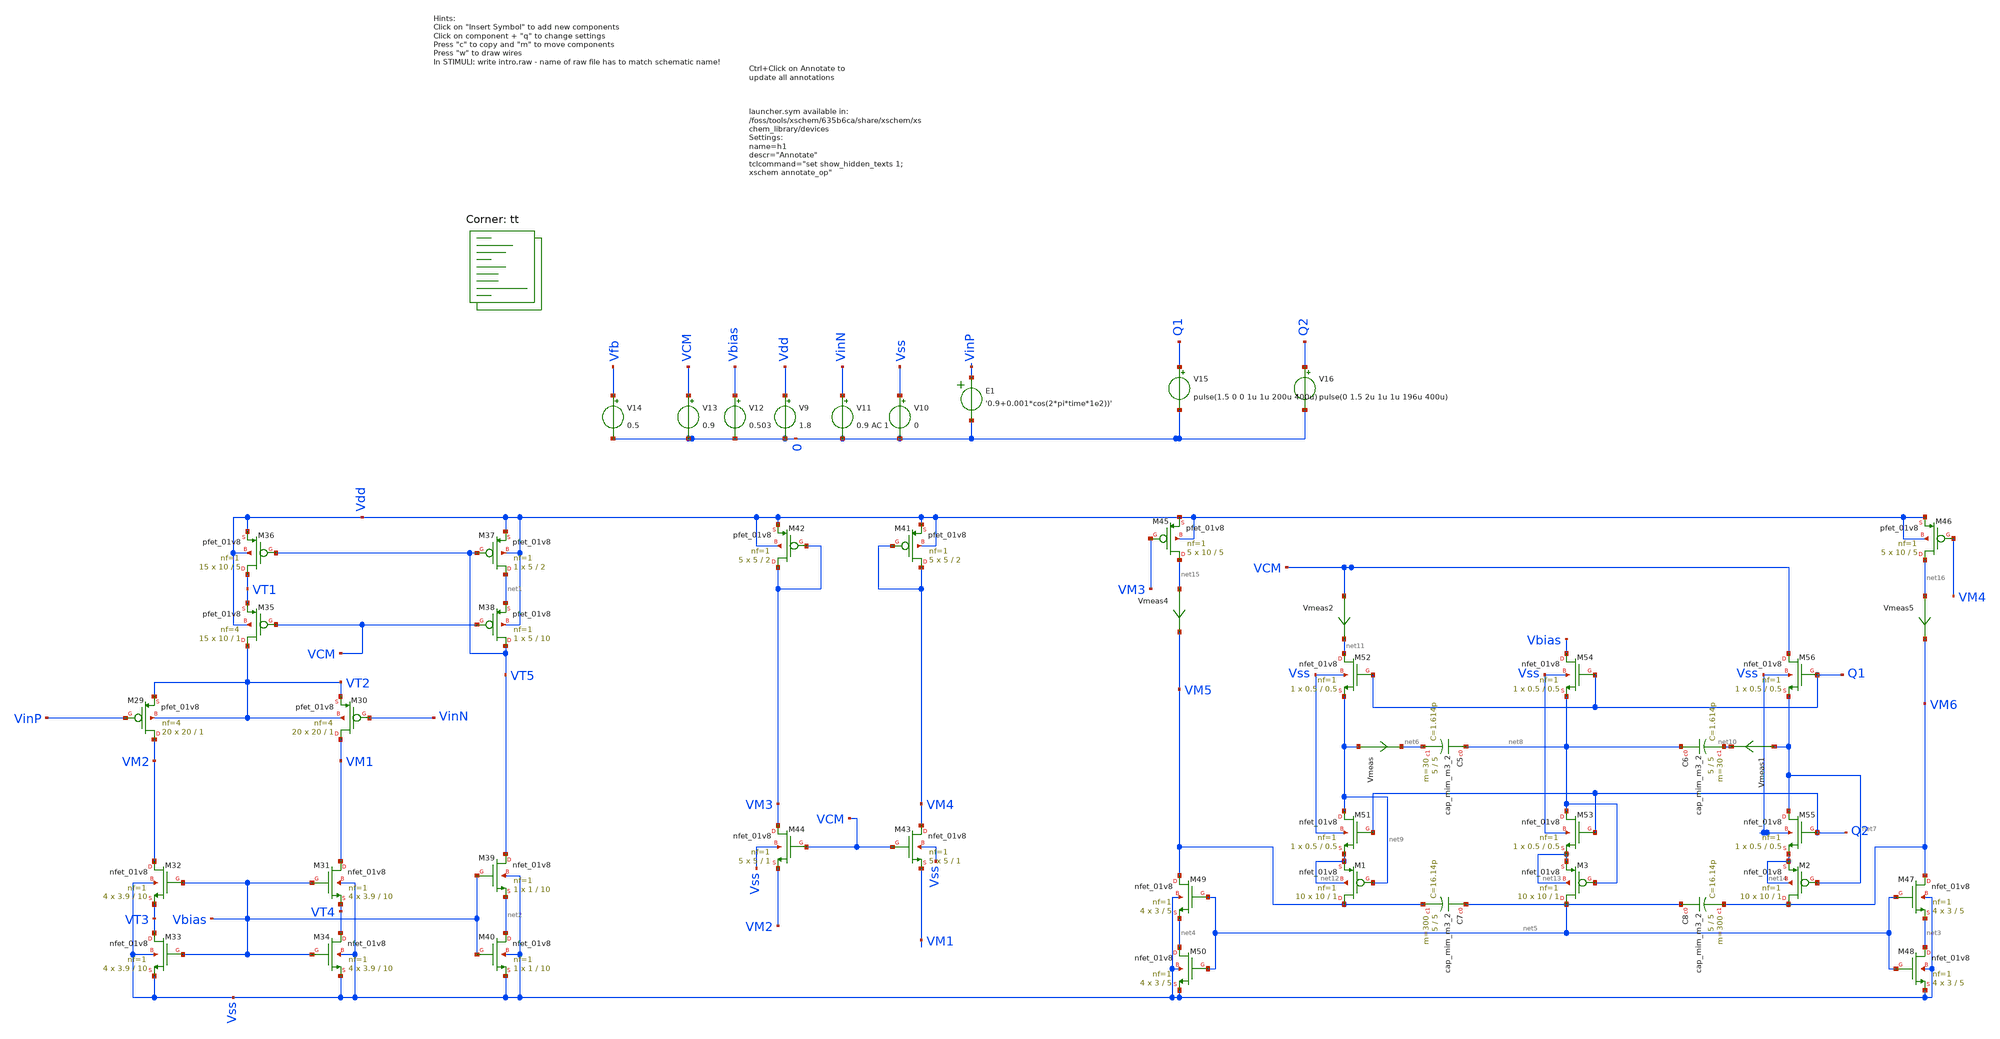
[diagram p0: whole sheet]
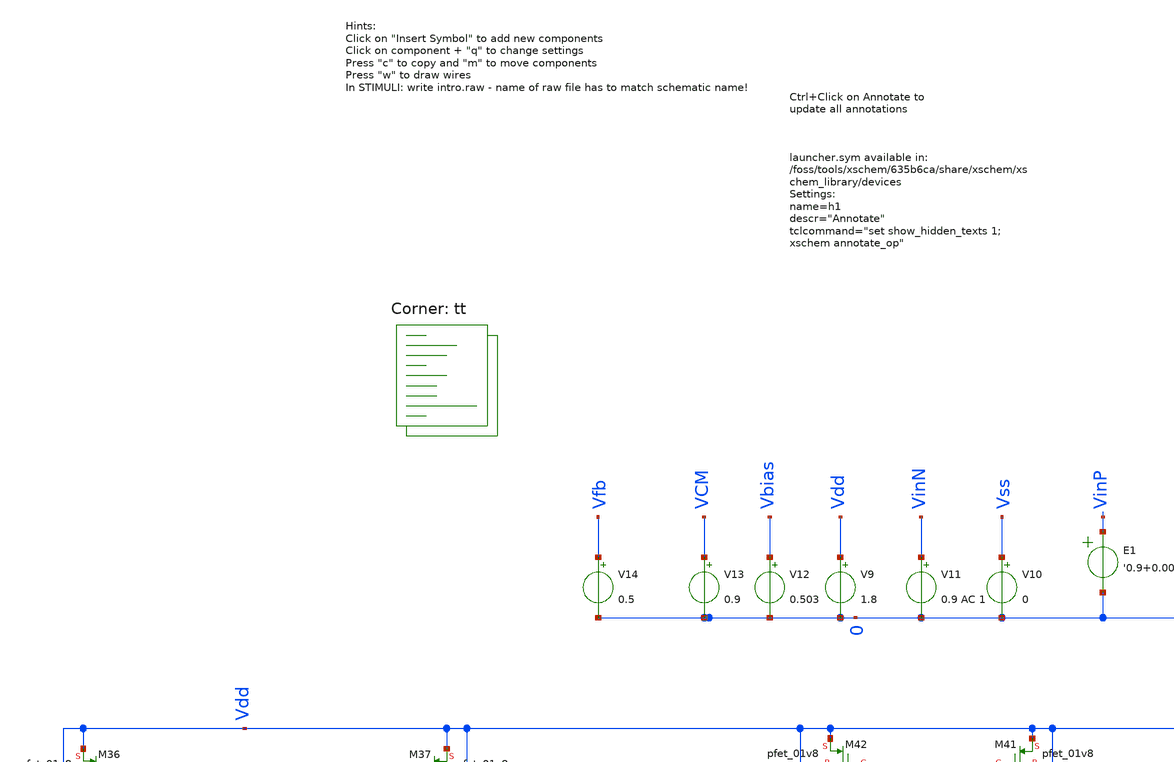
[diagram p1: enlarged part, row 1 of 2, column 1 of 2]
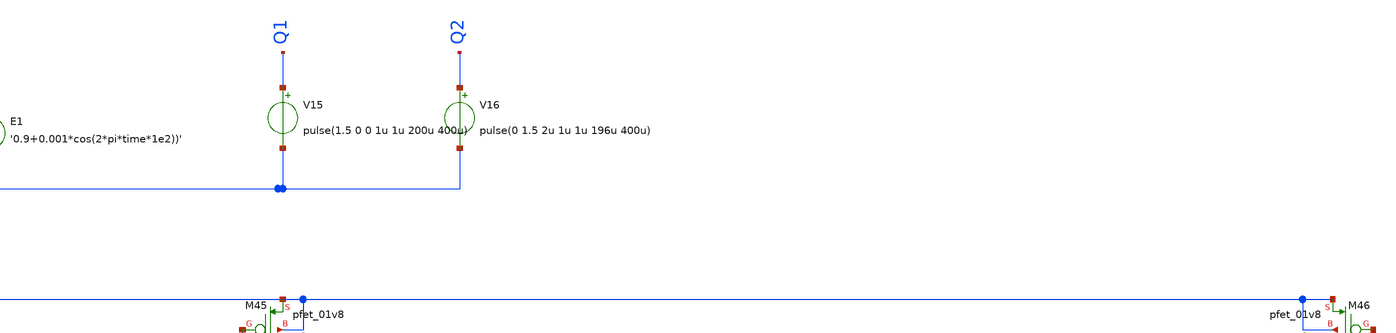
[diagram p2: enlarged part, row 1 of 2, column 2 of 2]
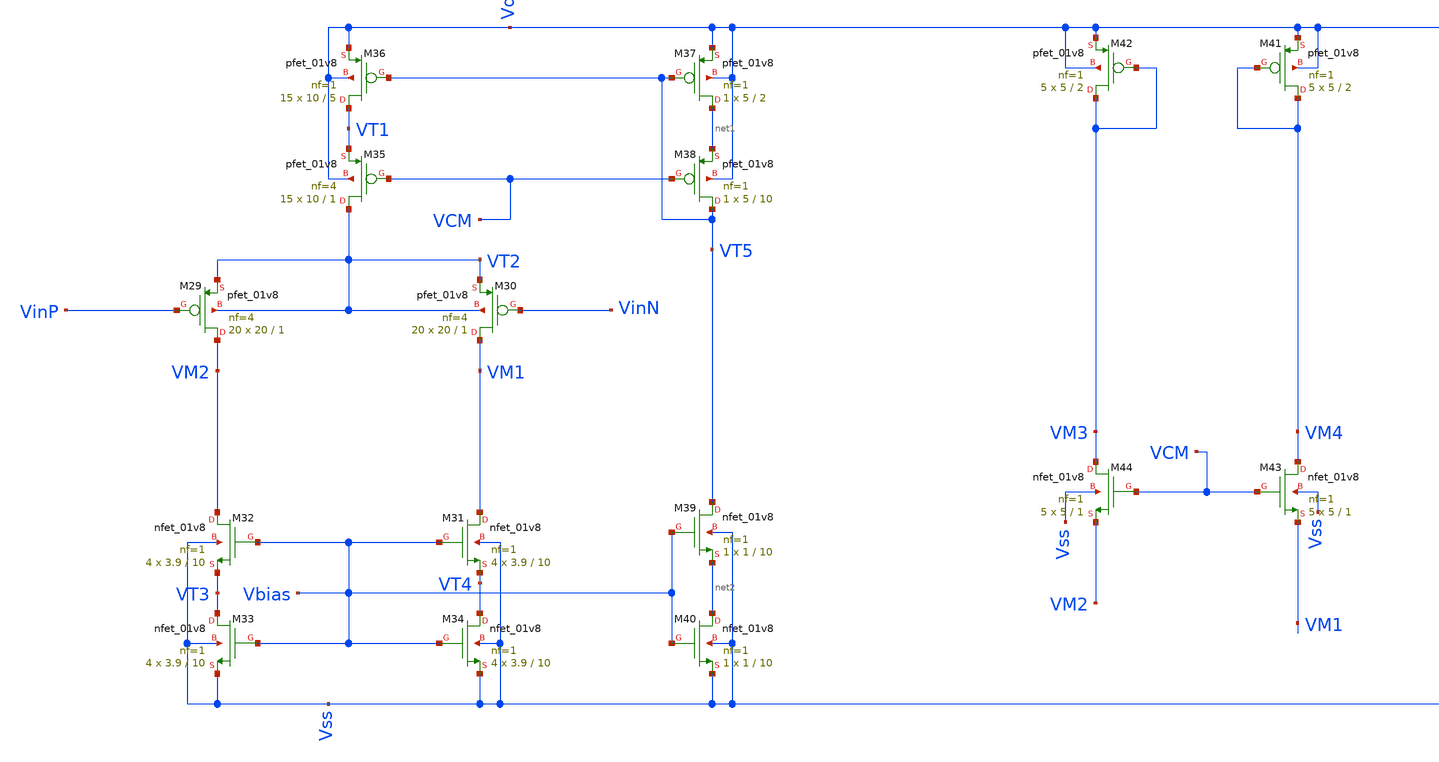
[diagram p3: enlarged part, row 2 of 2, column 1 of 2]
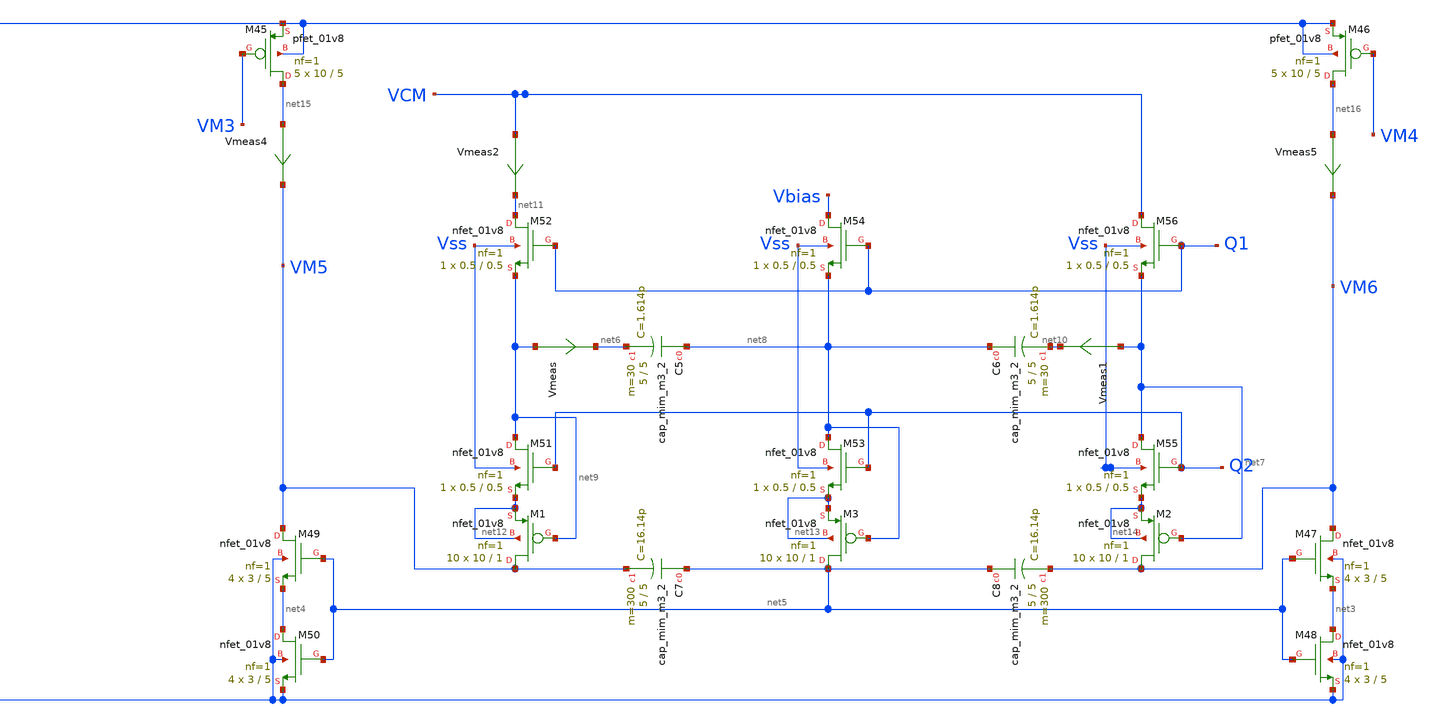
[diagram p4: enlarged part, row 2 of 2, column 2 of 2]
** sch_path: backup2.sch
**.subckt backup2
XM29 VM2 VinP VT2 VT2 sky130_fd_pr__pfet_01v8 L=1 W=20 nf=4 ad='int((nf+1)/2) * W/nf * 0.29' as='int((nf+2)/2) * W/nf * 0.29'
+ pd='2*int((nf+1)/2) * (W/nf + 0.29)' ps='2*int((nf+2)/2) * (W/nf + 0.29)' nrd='0.29 / W' nrs='0.29 / W'
+ sa=0 sb=0 sd=0 mult=20 m=20
XM30 VM1 VinN VT2 VT2 sky130_fd_pr__pfet_01v8 L=1 W=20 nf=4 ad='int((nf+1)/2) * W/nf * 0.29' as='int((nf+2)/2) * W/nf * 0.29'
+ pd='2*int((nf+1)/2) * (W/nf + 0.29)' ps='2*int((nf+2)/2) * (W/nf + 0.29)' nrd='0.29 / W' nrs='0.29 / W'
+ sa=0 sb=0 sd=0 mult=20 m=20
XM31 VM1 Vbias VT4 Vss sky130_fd_pr__nfet_01v8 L=10 W=3.9 nf=1 ad='int((nf+1)/2) * W/nf * 0.29' as='int((nf+2)/2) * W/nf * 0.29'
+ pd='2*int((nf+1)/2) * (W/nf + 0.29)' ps='2*int((nf+2)/2) * (W/nf + 0.29)' nrd='0.29 / W' nrs='0.29 / W'
+ sa=0 sb=0 sd=0 mult=4 m=4
XM32 VM2 Vbias VT3 Vss sky130_fd_pr__nfet_01v8 L=10 W=3.9 nf=1 ad='int((nf+1)/2) * W/nf * 0.29' as='int((nf+2)/2) * W/nf * 0.29'
+ pd='2*int((nf+1)/2) * (W/nf + 0.29)' ps='2*int((nf+2)/2) * (W/nf + 0.29)' nrd='0.29 / W' nrs='0.29 / W'
+ sa=0 sb=0 sd=0 mult=4 m=4
XM33 VT3 Vbias Vss Vss sky130_fd_pr__nfet_01v8 L=10 W=3.9 nf=1 ad='int((nf+1)/2) * W/nf * 0.29' as='int((nf+2)/2) * W/nf * 0.29'
+ pd='2*int((nf+1)/2) * (W/nf + 0.29)' ps='2*int((nf+2)/2) * (W/nf + 0.29)' nrd='0.29 / W' nrs='0.29 / W'
+ sa=0 sb=0 sd=0 mult=4 m=4
XM34 VT4 Vbias Vss Vss sky130_fd_pr__nfet_01v8 L=10 W=3.9 nf=1 ad='int((nf+1)/2) * W/nf * 0.29' as='int((nf+2)/2) * W/nf * 0.29'
+ pd='2*int((nf+1)/2) * (W/nf + 0.29)' ps='2*int((nf+2)/2) * (W/nf + 0.29)' nrd='0.29 / W' nrs='0.29 / W'
+ sa=0 sb=0 sd=0 mult=4 m=4
XM35 VT2 VCM VT1 Vdd sky130_fd_pr__pfet_01v8 L=1 W=10 nf=4 ad='int((nf+1)/2) * W/nf * 0.29' as='int((nf+2)/2) * W/nf * 0.29'
+ pd='2*int((nf+1)/2) * (W/nf + 0.29)' ps='2*int((nf+2)/2) * (W/nf + 0.29)' nrd='0.29 / W' nrs='0.29 / W'
+ sa=0 sb=0 sd=0 mult=15 m=15
XM36 VT1 VT5 Vdd Vdd sky130_fd_pr__pfet_01v8 L=5 W=10 nf=1 ad='int((nf+1)/2) * W/nf * 0.29' as='int((nf+2)/2) * W/nf * 0.29'
+ pd='2*int((nf+1)/2) * (W/nf + 0.29)' ps='2*int((nf+2)/2) * (W/nf + 0.29)' nrd='0.29 / W' nrs='0.29 / W'
+ sa=0 sb=0 sd=0 mult=15 m=15
XM37 net1 VT5 Vdd Vdd sky130_fd_pr__pfet_01v8 L=2 W=5 nf=1 ad='int((nf+1)/2) * W/nf * 0.29' as='int((nf+2)/2) * W/nf * 0.29'
+ pd='2*int((nf+1)/2) * (W/nf + 0.29)' ps='2*int((nf+2)/2) * (W/nf + 0.29)' nrd='0.29 / W' nrs='0.29 / W'
+ sa=0 sb=0 sd=0 mult=1 m=1
XM38 VT5 VCM net1 Vdd sky130_fd_pr__pfet_01v8 L=10 W=5 nf=1 ad='int((nf+1)/2) * W/nf * 0.29' as='int((nf+2)/2) * W/nf * 0.29'
+ pd='2*int((nf+1)/2) * (W/nf + 0.29)' ps='2*int((nf+2)/2) * (W/nf + 0.29)' nrd='0.29 / W' nrs='0.29 / W'
+ sa=0 sb=0 sd=0 mult=1 m=1
XM39 VT5 Vbias net2 Vss sky130_fd_pr__nfet_01v8 L=10 W=1 nf=1 ad='int((nf+1)/2) * W/nf * 0.29' as='int((nf+2)/2) * W/nf * 0.29'
+ pd='2*int((nf+1)/2) * (W/nf + 0.29)' ps='2*int((nf+2)/2) * (W/nf + 0.29)' nrd='0.29 / W' nrs='0.29 / W'
+ sa=0 sb=0 sd=0 mult=1 m=1
XM40 net2 Vbias Vss Vss sky130_fd_pr__nfet_01v8 L=10 W=1 nf=1 ad='int((nf+1)/2) * W/nf * 0.29' as='int((nf+2)/2) * W/nf * 0.29'
+ pd='2*int((nf+1)/2) * (W/nf + 0.29)' ps='2*int((nf+2)/2) * (W/nf + 0.29)' nrd='0.29 / W' nrs='0.29 / W'
+ sa=0 sb=0 sd=0 mult=1 m=1
XM41 VM4 VM4 Vdd Vdd sky130_fd_pr__pfet_01v8 L=2 W=5 nf=1 ad='int((nf+1)/2) * W/nf * 0.29' as='int((nf+2)/2) * W/nf * 0.29'
+ pd='2*int((nf+1)/2) * (W/nf + 0.29)' ps='2*int((nf+2)/2) * (W/nf + 0.29)' nrd='0.29 / W' nrs='0.29 / W'
+ sa=0 sb=0 sd=0 mult=5 m=5
XM42 VM3 VM3 Vdd Vdd sky130_fd_pr__pfet_01v8 L=2 W=5 nf=1 ad='int((nf+1)/2) * W/nf * 0.29' as='int((nf+2)/2) * W/nf * 0.29'
+ pd='2*int((nf+1)/2) * (W/nf + 0.29)' ps='2*int((nf+2)/2) * (W/nf + 0.29)' nrd='0.29 / W' nrs='0.29 / W'
+ sa=0 sb=0 sd=0 mult=5 m=5
XM43 VM4 VCM VM1 Vss sky130_fd_pr__nfet_01v8 L=1 W=5 nf=1 ad='int((nf+1)/2) * W/nf * 0.29' as='int((nf+2)/2) * W/nf * 0.29'
+ pd='2*int((nf+1)/2) * (W/nf + 0.29)' ps='2*int((nf+2)/2) * (W/nf + 0.29)' nrd='0.29 / W' nrs='0.29 / W'
+ sa=0 sb=0 sd=0 mult=5 m=5
XM44 VM3 VCM VM2 Vss sky130_fd_pr__nfet_01v8 L=1 W=5 nf=1 ad='int((nf+1)/2) * W/nf * 0.29' as='int((nf+2)/2) * W/nf * 0.29'
+ pd='2*int((nf+1)/2) * (W/nf + 0.29)' ps='2*int((nf+2)/2) * (W/nf + 0.29)' nrd='0.29 / W' nrs='0.29 / W'
+ sa=0 sb=0 sd=0 mult=5 m=5
XM45 net15 VM3 Vdd Vdd sky130_fd_pr__pfet_01v8 L=5 W=10 nf=1 ad='int((nf+1)/2) * W/nf * 0.29' as='int((nf+2)/2) * W/nf * 0.29'
+ pd='2*int((nf+1)/2) * (W/nf + 0.29)' ps='2*int((nf+2)/2) * (W/nf + 0.29)' nrd='0.29 / W' nrs='0.29 / W'
+ sa=0 sb=0 sd=0 mult=5 m=5
XM46 net16 VM4 Vdd Vdd sky130_fd_pr__pfet_01v8 L=5 W=10 nf=1 ad='int((nf+1)/2) * W/nf * 0.29' as='int((nf+2)/2) * W/nf * 0.29'
+ pd='2*int((nf+1)/2) * (W/nf + 0.29)' ps='2*int((nf+2)/2) * (W/nf + 0.29)' nrd='0.29 / W' nrs='0.29 / W'
+ sa=0 sb=0 sd=0 mult=5 m=5
XM47 VM6 net5 net3 Vss sky130_fd_pr__nfet_01v8 L=5 W=3 nf=1 ad='int((nf+1)/2) * W/nf * 0.29' as='int((nf+2)/2) * W/nf * 0.29'
+ pd='2*int((nf+1)/2) * (W/nf + 0.29)' ps='2*int((nf+2)/2) * (W/nf + 0.29)' nrd='0.29 / W' nrs='0.29 / W'
+ sa=0 sb=0 sd=0 mult=4 m=4
XM48 net3 net5 Vss Vss sky130_fd_pr__nfet_01v8 L=5 W=3 nf=1 ad='int((nf+1)/2) * W/nf * 0.29' as='int((nf+2)/2) * W/nf * 0.29'
+ pd='2*int((nf+1)/2) * (W/nf + 0.29)' ps='2*int((nf+2)/2) * (W/nf + 0.29)' nrd='0.29 / W' nrs='0.29 / W'
+ sa=0 sb=0 sd=0 mult=4 m=4
XM49 VM5 net5 net4 Vss sky130_fd_pr__nfet_01v8 L=5 W=3 nf=1 ad='int((nf+1)/2) * W/nf * 0.29' as='int((nf+2)/2) * W/nf * 0.29'
+ pd='2*int((nf+1)/2) * (W/nf + 0.29)' ps='2*int((nf+2)/2) * (W/nf + 0.29)' nrd='0.29 / W' nrs='0.29 / W'
+ sa=0 sb=0 sd=0 mult=4 m=4
XM50 net4 net5 Vss Vss sky130_fd_pr__nfet_01v8 L=5 W=3 nf=1 ad='int((nf+1)/2) * W/nf * 0.29' as='int((nf+2)/2) * W/nf * 0.29'
+ pd='2*int((nf+1)/2) * (W/nf + 0.29)' ps='2*int((nf+2)/2) * (W/nf + 0.29)' nrd='0.29 / W' nrs='0.29 / W'
+ sa=0 sb=0 sd=0 mult=4 m=4
E1 VinP 0 VOL=' '0.9+0.001*cos(2*pi*time*1e2))' '
V9 Vdd 0 1.8
V10 Vss 0 0
V11 VinN 0 0.9 AC 1
V12 Vbias 0 0.503
V13 VCM 0 0.9
V14 Vfb 0 0.5
XC5 net8 net6 sky130_fd_pr__cap_mim_m3_2 W=5 L=5 MF=30 m=30
XC6 net8 net10 sky130_fd_pr__cap_mim_m3_2 W=5 L=5 MF=30 m=30
XC7 net5 VM5 sky130_fd_pr__cap_mim_m3_2 W=5 L=5 MF=300 m=300
XC8 net5 VM6 sky130_fd_pr__cap_mim_m3_2 W=5 L=5 MF=300 m=300
XM51 net9 Q2 net12 Vss sky130_fd_pr__nfet_01v8 L=0.5 W=0.5 nf=1 ad='int((nf+1)/2) * W/nf * 0.29' as='int((nf+2)/2) * W/nf * 0.29'
+ pd='2*int((nf+1)/2) * (W/nf + 0.29)' ps='2*int((nf+2)/2) * (W/nf + 0.29)' nrd='0.29 / W' nrs='0.29 / W'
+ sa=0 sb=0 sd=0 mult=1 m=1
XM52 net11 Q1 net9 Vss sky130_fd_pr__nfet_01v8 L=0.5 W=0.5 nf=1 ad='int((nf+1)/2) * W/nf * 0.29' as='int((nf+2)/2) * W/nf * 0.29'
+ pd='2*int((nf+1)/2) * (W/nf + 0.29)' ps='2*int((nf+2)/2) * (W/nf + 0.29)' nrd='0.29 / W' nrs='0.29 / W'
+ sa=0 sb=0 sd=0 mult=1 m=1
XM53 net8 Q2 net13 Vss sky130_fd_pr__nfet_01v8 L=0.5 W=0.5 nf=1 ad='int((nf+1)/2) * W/nf * 0.29' as='int((nf+2)/2) * W/nf * 0.29'
+ pd='2*int((nf+1)/2) * (W/nf + 0.29)' ps='2*int((nf+2)/2) * (W/nf + 0.29)' nrd='0.29 / W' nrs='0.29 / W'
+ sa=0 sb=0 sd=0 mult=1 m=1
XM54 Vbias Q1 net8 Vss sky130_fd_pr__nfet_01v8 L=0.5 W=0.5 nf=1 ad='int((nf+1)/2) * W/nf * 0.29' as='int((nf+2)/2) * W/nf * 0.29'
+ pd='2*int((nf+1)/2) * (W/nf + 0.29)' ps='2*int((nf+2)/2) * (W/nf + 0.29)' nrd='0.29 / W' nrs='0.29 / W'
+ sa=0 sb=0 sd=0 mult=1 m=1
XM55 net7 Q2 net14 Vss sky130_fd_pr__nfet_01v8 L=0.5 W=0.5 nf=1 ad='int((nf+1)/2) * W/nf * 0.29' as='int((nf+2)/2) * W/nf * 0.29'
+ pd='2*int((nf+1)/2) * (W/nf + 0.29)' ps='2*int((nf+2)/2) * (W/nf + 0.29)' nrd='0.29 / W' nrs='0.29 / W'
+ sa=0 sb=0 sd=0 mult=1 m=1
XM56 VCM Q1 net7 Vss sky130_fd_pr__nfet_01v8 L=0.5 W=0.5 nf=1 ad='int((nf+1)/2) * W/nf * 0.29' as='int((nf+2)/2) * W/nf * 0.29'
+ pd='2*int((nf+1)/2) * (W/nf + 0.29)' ps='2*int((nf+2)/2) * (W/nf + 0.29)' nrd='0.29 / W' nrs='0.29 / W'
+ sa=0 sb=0 sd=0 mult=1 m=1
V15 Q1 0 pulse(1.5 0 0 1u 1u 200u 400u)
V16 Q2 0 pulse(0 1.5 2u 1u 1u 196u 400u)
Vmeas net9 net6 0
.save i(vmeas)
Vmeas1 net7 net10 0
.save i(vmeas1)
Vmeas2 VCM net11 0
.save i(vmeas2)
Vmeas4 net15 VM5 0
.save i(vmeas4)
Vmeas5 net16 VM6 0
.save i(vmeas5)
XM1 VM5 net9 net12 net12 sky130_fd_pr__nfet_01v8 L=1 W=10 nf=1 ad='int((nf+1)/2) * W/nf * 0.29' as='int((nf+2)/2) * W/nf * 0.29'
+ pd='2*int((nf+1)/2) * (W/nf + 0.29)' ps='2*int((nf+2)/2) * (W/nf + 0.29)' nrd='0.29 / W' nrs='0.29 / W'
+ sa=0 sb=0 sd=0 mult=10 m=10
XM2 VM6 net7 net14 net14 sky130_fd_pr__nfet_01v8 L=1 W=10 nf=1 ad='int((nf+1)/2) * W/nf * 0.29' as='int((nf+2)/2) * W/nf * 0.29'
+ pd='2*int((nf+1)/2) * (W/nf + 0.29)' ps='2*int((nf+2)/2) * (W/nf + 0.29)' nrd='0.29 / W' nrs='0.29 / W'
+ sa=0 sb=0 sd=0 mult=10 m=10
XM3 net5 net8 net13 net13 sky130_fd_pr__nfet_01v8 L=1 W=10 nf=1 ad='int((nf+1)/2) * W/nf * 0.29' as='int((nf+2)/2) * W/nf * 0.29'
+ pd='2*int((nf+1)/2) * (W/nf + 0.29)' ps='2*int((nf+2)/2) * (W/nf + 0.29)' nrd='0.29 / W' nrs='0.29 / W'
+ sa=0 sb=0 sd=0 mult=10 m=10
**** begin user architecture code


.options savecurrents
.control



save all
save @m.xm1.msky130_fd_pr__nfet_01v8_lvt[id]
save @m.xm1.msky130_fd_pr__pfet_01v8[id]
save @m.xm7.msky130_fd_pr__pfet_01v8[id]
save @m.xm1.msky130_fd_pr__nfet_01v8_lvt[vth]
save @m.xm1.msky130_fd_pr__nfet_01v8_lvt[vgs]
save @m.xm1.msky130_fd_pr__nfet_01v8_lvt[vds]
save @m.xm1.msky130_fd_pr__nfet_01v8_lvt[gm]
save @m.xm1.msky130_fd_pr__nfet_01v8_lvt[gds]
save @m.xm23.msky130_fd_pr__nfet_01v8[cgs]
save @m.xm15.msky130_fd_pr__nfet_01v8[cgs]

save @m.xm1.msky130_fd_pr__pfet_01v8[id]
save @m.xm2.msky130_fd_pr__pfet_01v8_lvt[id]
save @m.xm2.msky130_fd_pr__pfet_01v8_lvt[vth]
save @m.xm1.msky130_fd_pr__pfet_01v8[vgs]
save @m.xm2.msky130_fd_pr__pfet_01v8_lvt[vds]
save @m.xm2.msky130_fd_pr__pfet_01v8_lvt[gm]
save @m.xm2.msky130_fd_pr__pfet_01v8_lvt[gds]
save @m.xm2.msky130_fd_pr__pfet_01v8_lvt[cgs]

op
remzerovec
write intro.raw
*set appendwrite

*dc V1 0 1.8 0.01
*plot @m.xm1.msky130_fd_pr__nfet_01v8_lvt[id] @m.xm2.msky130_fd_pr__pfet_01v8_lvt[id]
*remzerovec
*write intro.raw

.endc
.control
tran 100u 1000m
save all
plot v(VM5)
plot v(VM6)-v(VM5)

*noise V(VM5,VM6) V1 dec 100 0.1 100
*print inoise_total onoise_total
*setplot noise1
*plot inoise_spectrum

.endc





.lib $::SKYWATER_MODELS/sky130.lib.spice tt
**** end user architecture code
**.ends
.end
